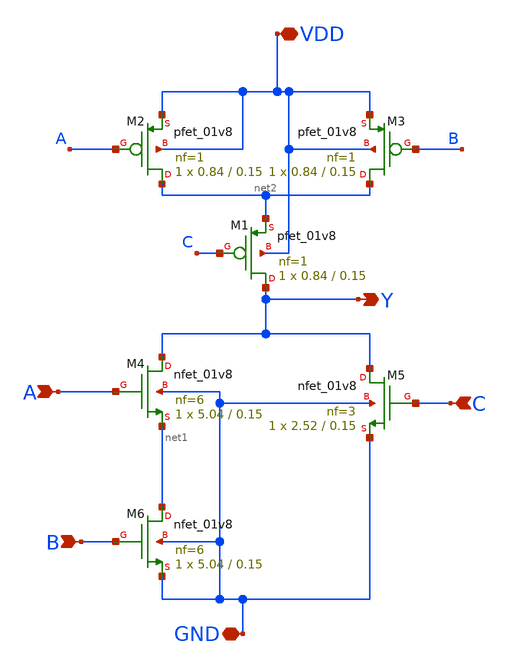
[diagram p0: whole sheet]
** sch_path: cells/AOI3X1/schematic/aoi3x1.sch
**.subckt aoi3x1 VDD GND A B C Y
*.iopin VDD
*.iopin GND
*.ipin A
*.ipin B
*.ipin C
*.opin Y
XM2 net2 A VDD VDD sky130_fd_pr__pfet_01v8 L=0.15 W=0.84 nf=1 ad='int((1 + 1)/2) * 0.84 / 1 * 0.29' as='int((1 + 2)/2) * 0.84 / 1 * 0.29'
+ pd='2*int((1 + 1)/2) * (0.84 / 1 + 0.29)' ps='2*int((1 + 2)/2) * (0.84 / 1 + 0.29)' nrd='0.29 / 0.84 '
+ nrs='0.29 / 0.84 ' sa=0 sb=0 sd=0 mult=1 m=1
XM3 net2 B VDD VDD sky130_fd_pr__pfet_01v8 L=0.15 W=0.84 nf=1 ad='int((1 + 1)/2) * 0.84 / 1 * 0.29' as='int((1 + 2)/2) * 0.84 / 1 * 0.29'
+ pd='2*int((1 + 1)/2) * (0.84 / 1 + 0.29)' ps='2*int((1 + 2)/2) * (0.84 / 1 + 0.29)' nrd='0.29 / 0.84 '
+ nrs='0.29 / 0.84 ' sa=0 sb=0 sd=0 mult=1 m=1
XM4 Y A net1 GND sky130_fd_pr__nfet_01v8 L=0.15 W=5.04 nf=6 ad='int((6 + 1)/2) * 5.04 / 6 * 0.29' as='int((6 + 2)/2) * 5.04 / 6 * 0.29'
+ pd='2*int((6 + 1)/2) * (5.04 / 6 + 0.29)' ps='2*int((6 + 2)/2) * (5.04 / 6 + 0.29)' nrd='0.29 / 5.04 '
+ nrs='0.29 / 5.04 ' sa=0 sb=0 sd=0 mult=1 m=1
XM5 Y C GND GND sky130_fd_pr__nfet_01v8 L=0.15 W=2.52 nf=3 ad='int((3 + 1)/2) * 2.52 / 3 * 0.29' as='int((3 + 2)/2) * 2.52 / 3 * 0.29'
+ pd='2*int((3 + 1)/2) * (2.52 / 3 + 0.29)' ps='2*int((3 + 2)/2) * (2.52 / 3 + 0.29)' nrd='0.29 / 2.52 '
+ nrs='0.29 / 2.52 ' sa=0 sb=0 sd=0 mult=1 m=1
XM1 Y C net2 VDD sky130_fd_pr__pfet_01v8 L=0.15 W=0.84 nf=1 ad='int((1 + 1)/2) * 0.84 / 1 * 0.29' as='int((1 + 2)/2) * 0.84 / 1 * 0.29'
+ pd='2*int((1 + 1)/2) * (0.84 / 1 + 0.29)' ps='2*int((1 + 2)/2) * (0.84 / 1 + 0.29)' nrd='0.29 / 0.84 '
+ nrs='0.29 / 0.84 ' sa=0 sb=0 sd=0 mult=1 m=1
XM6 net1 B GND GND sky130_fd_pr__nfet_01v8 L=0.15 W=5.04 nf=6 ad='int((6 + 1)/2) * 5.04 / 6 * 0.29' as='int((6 + 2)/2) * 5.04 / 6 * 0.29'
+ pd='2*int((6 + 1)/2) * (5.04 / 6 + 0.29)' ps='2*int((6 + 2)/2) * (5.04 / 6 + 0.29)' nrd='0.29 / 5.04 '
+ nrs='0.29 / 5.04 ' sa=0 sb=0 sd=0 mult=1 m=1
**.ends
.end
